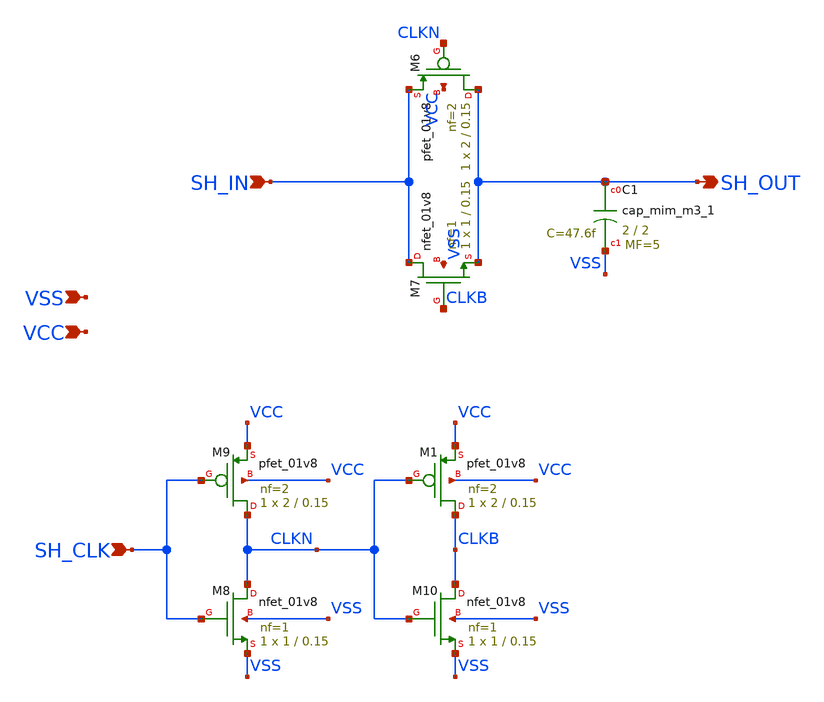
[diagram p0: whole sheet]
** sch_path: xschem/Sample_and_Hold.sch
**.subckt Sample_and_Hold SH_IN SH_CLK SH_OUT VSS VCC
*.ipin SH_IN
*.ipin SH_CLK
*.opin SH_OUT
*.ipin VSS
*.ipin VCC
XC1 SH_OUT VSS sky130_fd_pr__cap_mim_m3_1 W=2 L=2 MF=5 m=5
XM6 SH_OUT CLKN SH_IN VCC sky130_fd_pr__pfet_01v8 L=0.15 W=2 nf=2 ad='int((nf+1)/2) * W/nf * 0.29' as='int((nf+2)/2) * W/nf * 0.29'
+ pd='2*int((nf+1)/2) * (W/nf + 0.29)' ps='2*int((nf+2)/2) * (W/nf + 0.29)' nrd='0.29 / W' nrs='0.29 / W'
+ sa=0 sb=0 sd=0 mult=1 m=1
XM7 SH_IN CLKB SH_OUT VSS sky130_fd_pr__nfet_01v8 L=0.15 W=1 nf=1 ad='int((nf+1)/2) * W/nf * 0.29' as='int((nf+2)/2) * W/nf * 0.29'
+ pd='2*int((nf+1)/2) * (W/nf + 0.29)' ps='2*int((nf+2)/2) * (W/nf + 0.29)' nrd='0.29 / W' nrs='0.29 / W'
+ sa=0 sb=0 sd=0 mult=1 m=1
XM8 CLKN SH_CLK VSS VSS sky130_fd_pr__nfet_01v8 L=0.15 W=1 nf=1 ad='int((nf+1)/2) * W/nf * 0.29' as='int((nf+2)/2) * W/nf * 0.29'
+ pd='2*int((nf+1)/2) * (W/nf + 0.29)' ps='2*int((nf+2)/2) * (W/nf + 0.29)' nrd='0.29 / W' nrs='0.29 / W'
+ sa=0 sb=0 sd=0 mult=1 m=1
XM9 CLKN SH_CLK VCC VCC sky130_fd_pr__pfet_01v8 L=0.15 W=2 nf=2 ad='int((nf+1)/2) * W/nf * 0.29' as='int((nf+2)/2) * W/nf * 0.29'
+ pd='2*int((nf+1)/2) * (W/nf + 0.29)' ps='2*int((nf+2)/2) * (W/nf + 0.29)' nrd='0.29 / W' nrs='0.29 / W'
+ sa=0 sb=0 sd=0 mult=1 m=1
XM10 CLKB CLKN VSS VSS sky130_fd_pr__nfet_01v8 L=0.15 W=1 nf=1 ad='int((nf+1)/2) * W/nf * 0.29' as='int((nf+2)/2) * W/nf * 0.29'
+ pd='2*int((nf+1)/2) * (W/nf + 0.29)' ps='2*int((nf+2)/2) * (W/nf + 0.29)' nrd='0.29 / W' nrs='0.29 / W'
+ sa=0 sb=0 sd=0 mult=1 m=1
XM1 CLKB CLKN VCC VCC sky130_fd_pr__pfet_01v8 L=0.15 W=2 nf=2 ad='int((nf+1)/2) * W/nf * 0.29' as='int((nf+2)/2) * W/nf * 0.29'
+ pd='2*int((nf+1)/2) * (W/nf + 0.29)' ps='2*int((nf+2)/2) * (W/nf + 0.29)' nrd='0.29 / W' nrs='0.29 / W'
+ sa=0 sb=0 sd=0 mult=1 m=1
**.ends
.end
